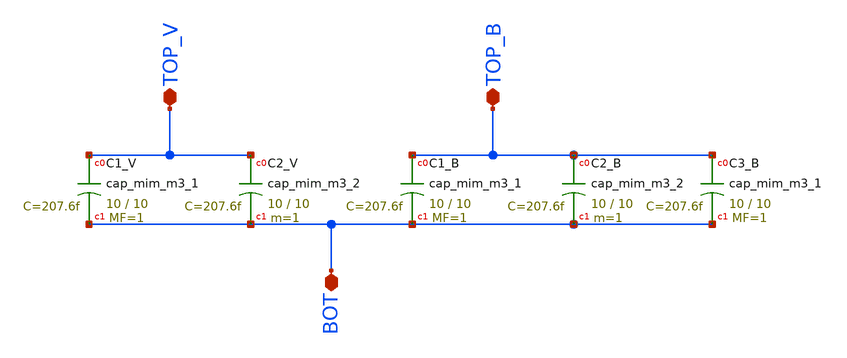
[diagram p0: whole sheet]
** sch_path: CAPOSC_v3p1.sch
**.subckt CAPOSC_v3p1 TOP_V TOP_B BOT
*.iopin TOP_V
*.iopin TOP_B
*.iopin BOT
XC1_V TOP_V BOT sky130_fd_pr__cap_mim_m3_1 W=10 L=10 MF=1 m=1
XC2_V TOP_V BOT sky130_fd_pr__cap_mim_m3_2 W=10 L=10 MF=1 m=1
XC1_B TOP_B BOT sky130_fd_pr__cap_mim_m3_1 W=10 L=10 MF=1 m=1
XC2_B TOP_B BOT sky130_fd_pr__cap_mim_m3_2 W=10 L=10 MF=1 m=1
XC3_B TOP_B BOT sky130_fd_pr__cap_mim_m3_1 W=10 L=10 MF=1 m=1
**.ends
.end
